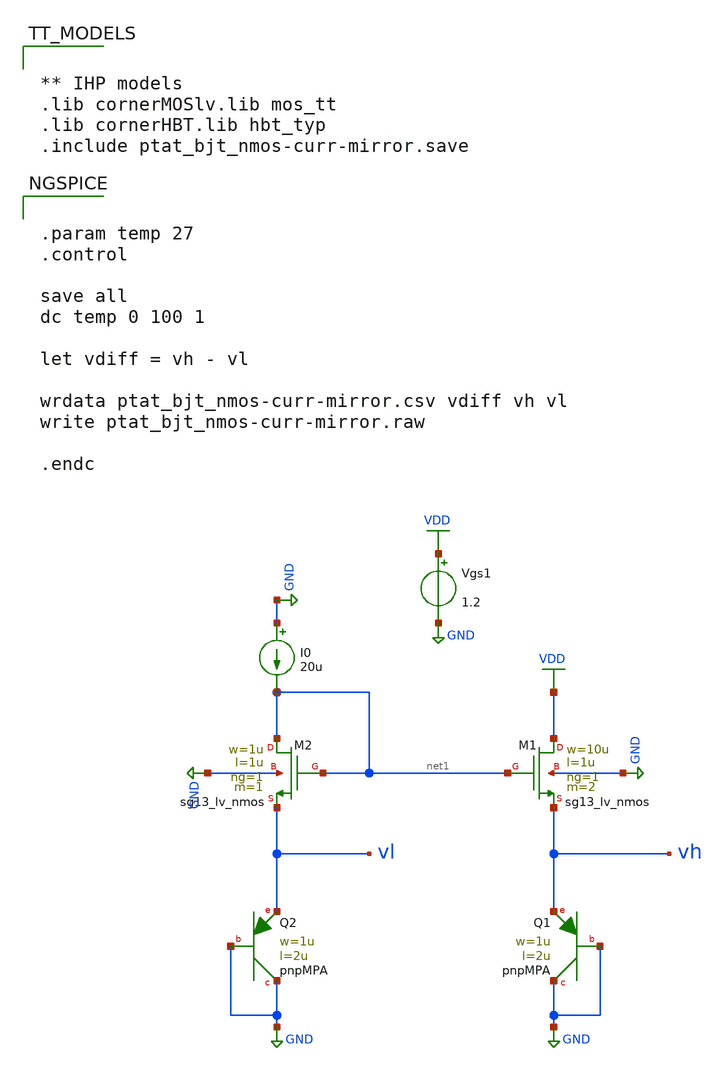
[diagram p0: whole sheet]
** sch_path: TempSensor/design_data/xschem/ptat_bjt_nmos-curr-mirror.sch
* Copyright 2023 IHP PDK Authors
**.subckt ptat_bjt_nmos-curr-mirror
XQ1 GND GND vh pnpMPA a=2p p=6u m=1
XQ2 GND GND vl pnpMPA a=2p p=6u m=1
XM2 net1 net1 vl GND sg13_lv_nmos w=1u l=1u ng=1 m=1 mm_ok=1
I0 GND net1 20u
Vgs1 VDD GND 1.2
XM1 VDD net1 vh GND sg13_lv_nmos w=10u l=1u ng=1 m=2 mm_ok=1
**** begin user architecture code


.param temp 27
.control

save all
dc temp 0 100 1

let vdiff = vh - vl

wrdata ptat_bjt_nmos-curr-mirror.csv vdiff vh vl
write ptat_bjt_nmos-curr-mirror.raw

.endc




** IHP models
.lib cornerMOSlv.lib mos_tt
.lib cornerHBT.lib hbt_typ
.include ptat_bjt_nmos-curr-mirror.save


**** end user architecture code
**.ends
.GLOBAL GND
.GLOBAL VDD
.end
